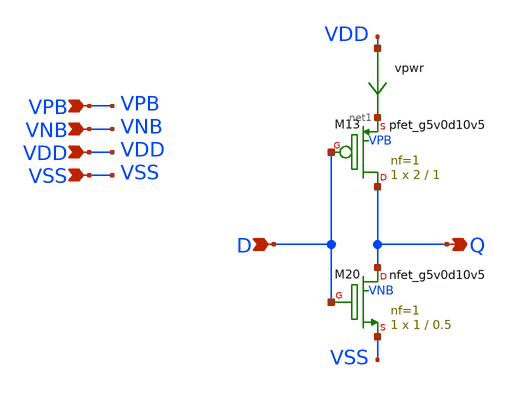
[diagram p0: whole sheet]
** sch_path: xschem/pll_inv2_hv.sch
**.subckt pll_inv2_hv Q D VDD VPB VNB VSS
*.opin Q
*.ipin D
*.ipin VDD
*.ipin VPB
*.ipin VNB
*.ipin VSS
vpwr VDD net1 0
.save i(vpwr)
XM13 Q D net1 VPB sky130_fd_pr__pfet_g5v0d10v5 L=1 W=2 nf=1 ad='int((nf+1)/2) * W/nf * 0.29' as='int((nf+2)/2) * W/nf * 0.29'
+ pd='2*int((nf+1)/2) * (W/nf + 0.29)' ps='2*int((nf+2)/2) * (W/nf + 0.29)' nrd='0.29 / W' nrs='0.29 / W'
+ sa=0 sb=0 sd=0 mult=1 m=1
XM20 Q D VSS VNB sky130_fd_pr__nfet_g5v0d10v5 L=0.5 W=1 nf=1 ad='int((nf+1)/2) * W/nf * 0.29' as='int((nf+2)/2) * W/nf * 0.29'
+ pd='2*int((nf+1)/2) * (W/nf + 0.29)' ps='2*int((nf+2)/2) * (W/nf + 0.29)' nrd='0.29 / W' nrs='0.29 / W'
+ sa=0 sb=0 sd=0 mult=1 m=1
**.ends
.end
